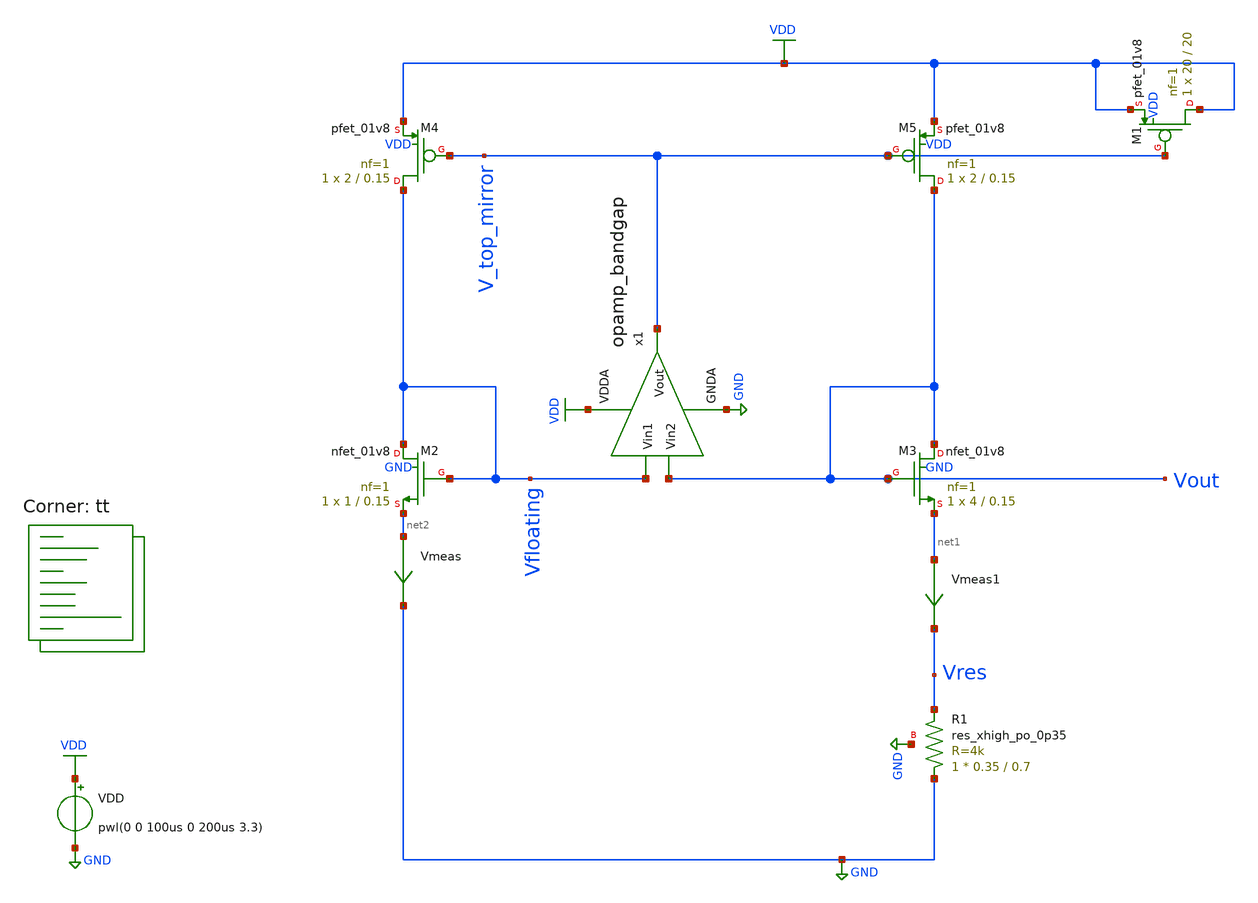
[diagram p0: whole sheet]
** sch_path: projects/pll/bandgapref/xschem_ngspice/mos_bandgap7.sch
**.subckt mos_bandgap7
XM2 Vfloating Vfloating net2 GND sky130_fd_pr__nfet_01v8 L=0.15 W=1 nf=1 ad='int((nf+1)/2) * W/nf * 0.29'
+ as='int((nf+2)/2) * W/nf * 0.29' pd='2*int((nf+1)/2) * (W/nf + 0.29)' ps='2*int((nf+2)/2) * (W/nf + 0.29)'
+ nrd='0.29 / W' nrs='0.29 / W' sa=0 sb=0 sd=0 mult=1 m=1
XM3 Vout Vout net1 GND sky130_fd_pr__nfet_01v8 L=0.15 W=4 nf=1 ad='int((nf+1)/2) * W/nf * 0.29' as='int((nf+2)/2) * W/nf * 0.29'
+ pd='2*int((nf+1)/2) * (W/nf + 0.29)' ps='2*int((nf+2)/2) * (W/nf + 0.29)' nrd='0.29 / W' nrs='0.29 / W'
+ sa=0 sb=0 sd=0 mult=1 m=1
XM4 Vfloating V_top_mirror VDD VDD sky130_fd_pr__pfet_01v8 L=0.15 W=2 nf=1 ad='int((nf+1)/2) * W/nf * 0.29'
+ as='int((nf+2)/2) * W/nf * 0.29' pd='2*int((nf+1)/2) * (W/nf + 0.29)' ps='2*int((nf+2)/2) * (W/nf + 0.29)'
+ nrd='0.29 / W' nrs='0.29 / W' sa=0 sb=0 sd=0 mult=1 m=1
XM5 Vout V_top_mirror VDD VDD sky130_fd_pr__pfet_01v8 L=0.15 W=2 nf=1 ad='int((nf+1)/2) * W/nf * 0.29'
+ as='int((nf+2)/2) * W/nf * 0.29' pd='2*int((nf+1)/2) * (W/nf + 0.29)' ps='2*int((nf+2)/2) * (W/nf + 0.29)'
+ nrd='0.29 / W' nrs='0.29 / W' sa=0 sb=0 sd=0 mult=1 m=1
VDD VDD GND pwl(0 0 100us 0 200us 3.3)
Vmeas net2 GND 0
.save i(vmeas)
Vmeas1 net1 Vres 0
.save i(vmeas1)
XR1 GND Vres GND sky130_fd_pr__res_xhigh_po_0p35 L=0.7 mult=1 m=1
x1 VDD V_top_mirror Vout Vfloating GND opamp_bandgap
XM1 VDD V_top_mirror VDD VDD sky130_fd_pr__pfet_01v8 L=20 W=20 nf=1 ad='int((nf+1)/2) * W/nf * 0.29'
+ as='int((nf+2)/2) * W/nf * 0.29' pd='2*int((nf+1)/2) * (W/nf + 0.29)' ps='2*int((nf+2)/2) * (W/nf + 0.29)'
+ nrd='0.29 / W' nrs='0.29 / W' sa=0 sb=0 sd=0 mult=1 m=1
**** begin user architecture code
.lib $::SKYWATER_MODELS/sky130.lib.spice tt



.option method=gear
.option wnflag=1
.option savecurrents

*  .param VDDGAUSS = agauss(3.3, 0.05, 1)
*  .param VDD = VDDGAUSS
** use following line to remove VCC variations
* .param VDD = 3.3

.control
save all
op
dc VDD 0 3.3 0.1
remzerovec
write mos_bandgap7.raw
set appendwrite
.endc



**** end user architecture code
**.ends

* expanding   symbol:
*+  /foss/designs/my_design/projects/pll/bandgapref/xschem_ngspice/opamp_bandgap.sym # of pins=5
** sym_path: projects/pll/bandgapref/xschem_ngspice/opamp_bandgap.sym
** sch_path: projects/pll/bandgapref/xschem_ngspice/opamp_bandgap.sch
.subckt opamp_bandgap VDDA Vout Vin2 Vin1 GNDA
*.ipin Vin1
*.opin Vout
*.ipin Vin2
*.ipin GNDA
*.ipin VDDA
XM2 net1 Vin1 net2 GNDA sky130_fd_pr__nfet_01v8 L=0.15 W=1 nf=1 ad='int((nf+1)/2) * W/nf * 0.29' as='int((nf+2)/2) * W/nf * 0.29'
+ pd='2*int((nf+1)/2) * (W/nf + 0.29)' ps='2*int((nf+2)/2) * (W/nf + 0.29)' nrd='0.29 / W' nrs='0.29 / W'
+ sa=0 sb=0 sd=0 mult=1 m=1
XM3 Vout Vin2 net2 GNDA sky130_fd_pr__nfet_01v8 L=0.15 W=1 nf=1 ad='int((nf+1)/2) * W/nf * 0.29' as='int((nf+2)/2) * W/nf * 0.29'
+ pd='2*int((nf+1)/2) * (W/nf + 0.29)' ps='2*int((nf+2)/2) * (W/nf + 0.29)' nrd='0.29 / W' nrs='0.29 / W'
+ sa=0 sb=0 sd=0 mult=1 m=1
XM4 net1 net1 VDDA VDDA sky130_fd_pr__pfet_01v8 L=0.15 W=2 nf=1 ad='int((nf+1)/2) * W/nf * 0.29' as='int((nf+2)/2) * W/nf * 0.29'
+ pd='2*int((nf+1)/2) * (W/nf + 0.29)' ps='2*int((nf+2)/2) * (W/nf + 0.29)' nrd='0.29 / W' nrs='0.29 / W'
+ sa=0 sb=0 sd=0 mult=1 m=1
XM5 Vout net1 VDDA VDDA sky130_fd_pr__pfet_01v8 L=0.15 W=2 nf=1 ad='int((nf+1)/2) * W/nf * 0.29' as='int((nf+2)/2) * W/nf * 0.29'
+ pd='2*int((nf+1)/2) * (W/nf + 0.29)' ps='2*int((nf+2)/2) * (W/nf + 0.29)' nrd='0.29 / W' nrs='0.29 / W'
+ sa=0 sb=0 sd=0 mult=1 m=1
XM1 net2 net2 GNDA GNDA sky130_fd_pr__nfet_01v8 L=0.15 W=1 nf=1 ad='int((nf+1)/2) * W/nf * 0.29' as='int((nf+2)/2) * W/nf * 0.29'
+ pd='2*int((nf+1)/2) * (W/nf + 0.29)' ps='2*int((nf+2)/2) * (W/nf + 0.29)' nrd='0.29 / W' nrs='0.29 / W'
+ sa=0 sb=0 sd=0 mult=1 m=1
.ends

.GLOBAL VDD
.GLOBAL GND
.end
